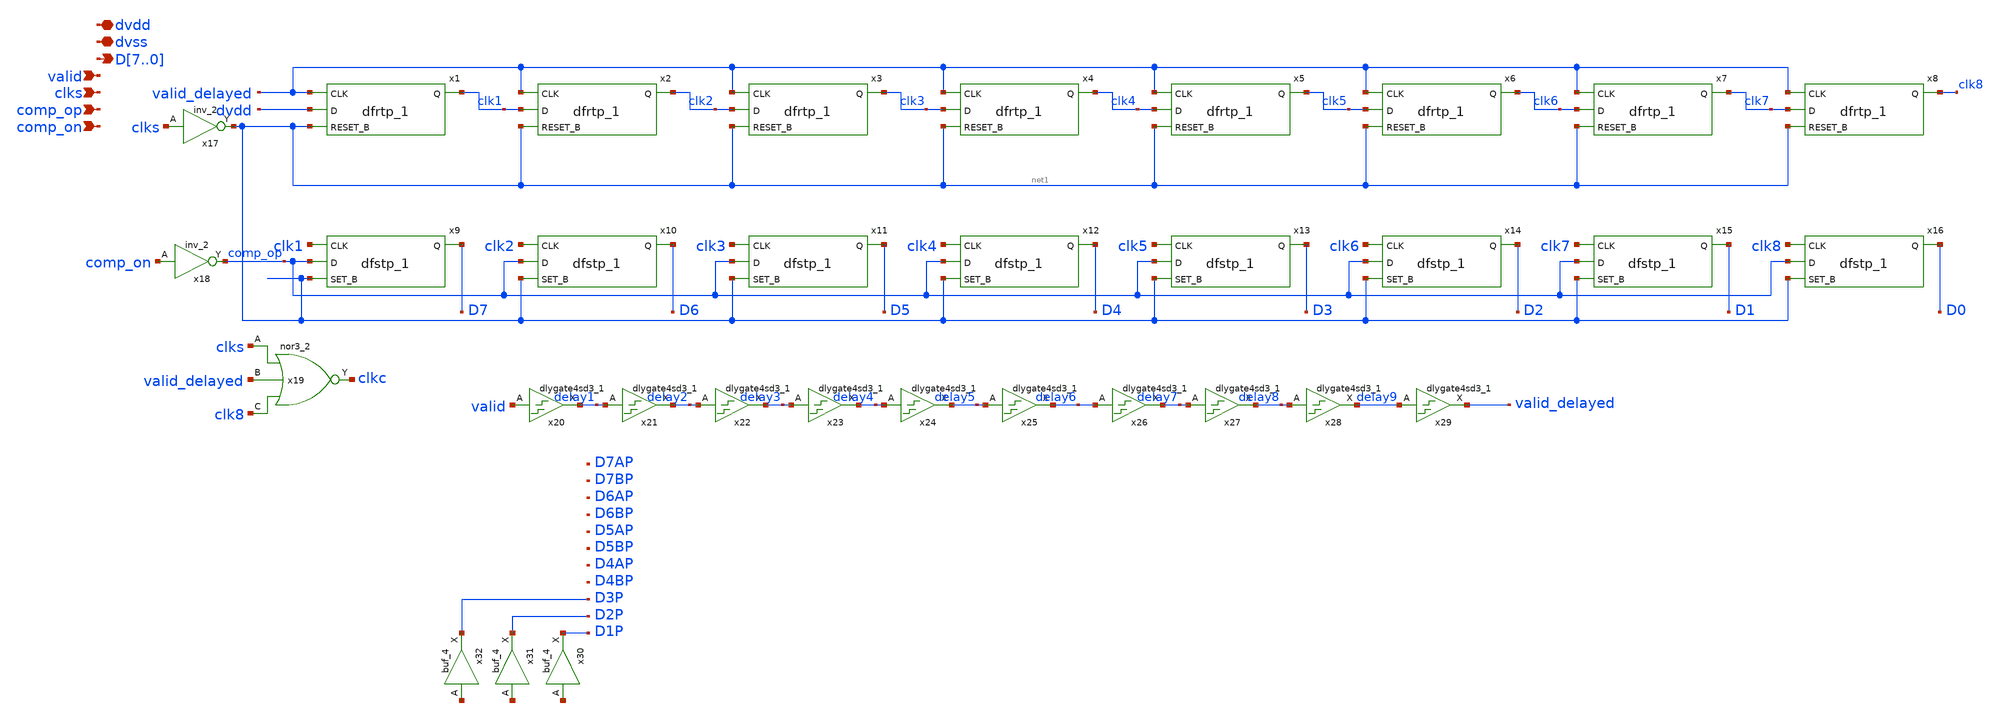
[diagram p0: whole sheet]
** sch_path: xschem/sar-adc/sarlogic.sch
**.subckt sarlogic valid clks comp_op D7,D6,D5,D4,D3,D2,D1,D0 dvdd dvss comp_on
*.ipin valid
*.ipin clks
*.ipin comp_op
*.opin D7,D6,D5,D4,D3,D2,D1,D0
*.iopin dvdd
*.iopin dvss
*.ipin comp_on
x1 valid_delayed dvdd net1 dvss dvss dvdd dvdd clk1 sky130_fd_sc_hd__dfrtp_1
x2 valid_delayed clk1 net1 dvss dvss dvdd dvdd clk2 sky130_fd_sc_hd__dfrtp_1
x3 valid_delayed clk2 net1 dvss dvss dvdd dvdd clk3 sky130_fd_sc_hd__dfrtp_1
x4 valid_delayed clk3 net1 dvss dvss dvdd dvdd clk4 sky130_fd_sc_hd__dfrtp_1
x5 valid_delayed clk4 net1 dvss dvss dvdd dvdd clk5 sky130_fd_sc_hd__dfrtp_1
x6 valid_delayed clk5 net1 dvss dvss dvdd dvdd clk6 sky130_fd_sc_hd__dfrtp_1
x7 valid_delayed clk6 net1 dvss dvss dvdd dvdd clk7 sky130_fd_sc_hd__dfrtp_1
x8 valid_delayed clk7 net1 dvss dvss dvdd dvdd clk8 sky130_fd_sc_hd__dfrtp_1
x17 clks dvss dvss dvdd dvdd net1 sky130_fd_sc_hd__inv_2
x9 clk1 comp_op net1 dvss dvss dvdd dvdd D7 sky130_fd_sc_hd__dfstp_1
x10 clk2 comp_op net1 dvss dvss dvdd dvdd D6 sky130_fd_sc_hd__dfstp_1
x11 clk3 comp_op net1 dvss dvss dvdd dvdd D5 sky130_fd_sc_hd__dfstp_1
x12 clk4 comp_op net1 dvss dvss dvdd dvdd D4 sky130_fd_sc_hd__dfstp_1
x13 clk5 comp_op net1 dvss dvss dvdd dvdd D3 sky130_fd_sc_hd__dfstp_1
x14 clk6 comp_op net1 dvss dvss dvdd dvdd D2 sky130_fd_sc_hd__dfstp_1
x15 clk7 comp_op net1 dvss dvss dvdd dvdd D1 sky130_fd_sc_hd__dfstp_1
x16 clk8 comp_op net1 dvss dvss dvdd dvdd D0 sky130_fd_sc_hd__dfstp_1
x18 comp_on dvss dvss dvdd dvdd comp_op sky130_fd_sc_hd__inv_2
x19 clks valid_delayed clk8 VGND VNB VPB VPWR clkc sky130_fd_sc_hd__nor3_2
x20 valid 0 0 dvdd dvdd delay1 sky130_fd_sc_hd__dlygate4sd3_1
x21 delay1 0 0 dvdd dvdd delay2 sky130_fd_sc_hd__dlygate4sd3_1
x22 delay2 0 0 dvdd dvdd delay3 sky130_fd_sc_hd__dlygate4sd3_1
x23 delay3 0 0 dvdd dvdd delay4 sky130_fd_sc_hd__dlygate4sd3_1
x24 delay4 0 0 dvdd dvdd delay5 sky130_fd_sc_hd__dlygate4sd3_1
x25 delay5 0 0 dvdd dvdd delay6 sky130_fd_sc_hd__dlygate4sd3_1
x26 delay6 0 0 dvdd dvdd delay7 sky130_fd_sc_hd__dlygate4sd3_1
x27 delay7 0 0 dvdd dvdd delay8 sky130_fd_sc_hd__dlygate4sd3_1
x28 delay8 0 0 dvdd dvdd delay9 sky130_fd_sc_hd__dlygate4sd3_1
x29 delay9 0 0 dvdd dvdd valid_delayed sky130_fd_sc_hd__dlygate4sd3_1
x30 net2 VGND VNB VPB VPWR D1P sky130_fd_sc_hd__buf_4
x31 net3 VGND VNB VPB VPWR D2P sky130_fd_sc_hd__buf_4
x32 net4 VGND VNB VPB VPWR D3P sky130_fd_sc_hd__buf_4
**.ends
.end
